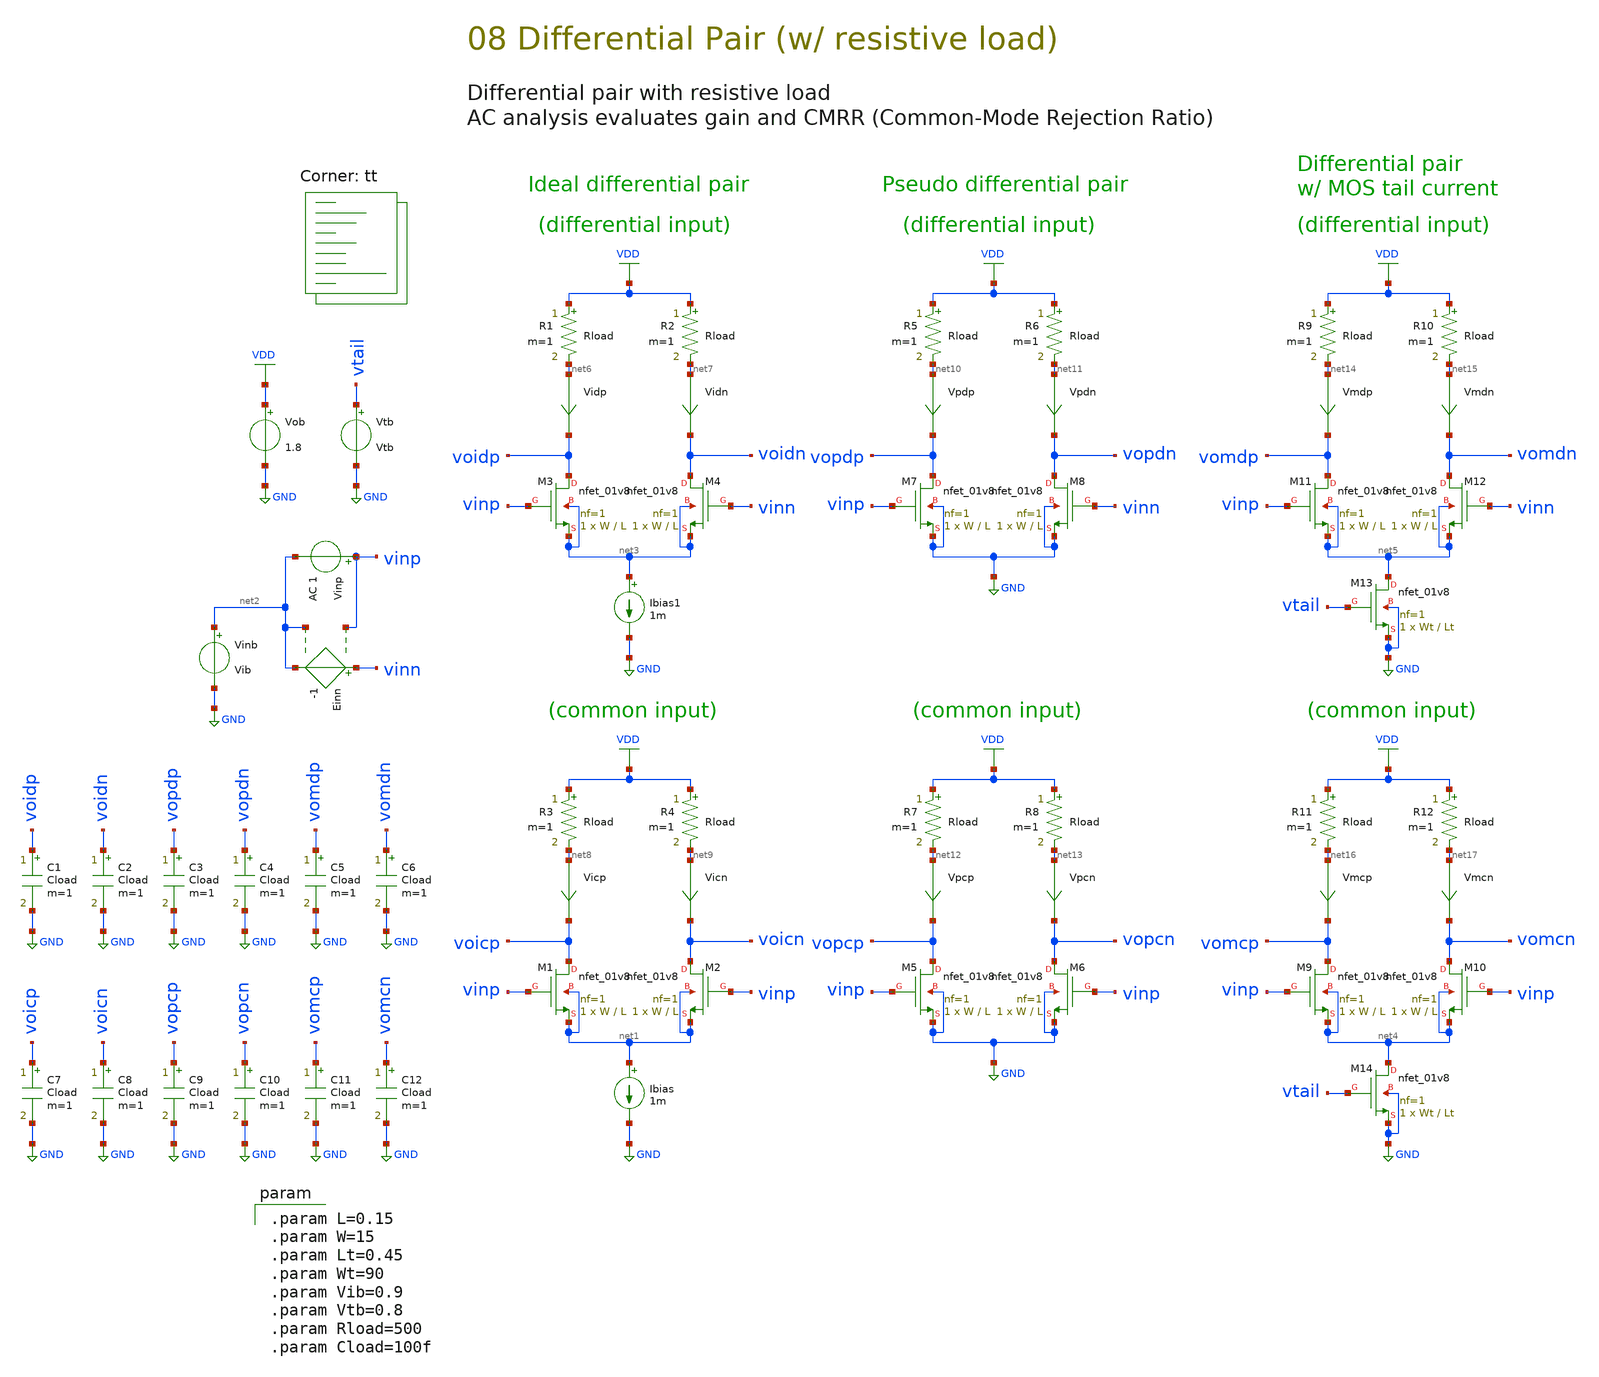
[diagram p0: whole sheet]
** sch_path: 08-b_diff-pair.sch
**.subckt 08-b_diff-pair
Vob VDD GND 1.8
XM1 voicp vinp net1 net1 sky130_fd_pr__nfet_01v8 L=L W=W nf=1 ad='int((1 + 1)/2) * W / 1 * 0.29' as='int((1 + 2)/2) * W / 1 * 0.29'
+ pd='2*int((1 + 1)/2) * (W / 1 + 0.29)' ps='2*int((1 + 2)/2) * (W / 1 + 0.29)' nrd='0.29 / W ' nrs='0.29 / W '
+ sa=0 sb=0 sd=0 mult=1 m=1
Vicn net9 voicn 0
.save i(vicn)
XM2 voicn vinp net1 net1 sky130_fd_pr__nfet_01v8 L=L W=W nf=1 ad='int((1 + 1)/2) * W / 1 * 0.29' as='int((1 + 2)/2) * W / 1 * 0.29'
+ pd='2*int((1 + 1)/2) * (W / 1 + 0.29)' ps='2*int((1 + 2)/2) * (W / 1 + 0.29)' nrd='0.29 / W ' nrs='0.29 / W '
+ sa=0 sb=0 sd=0 mult=1 m=1
Vinb net2 GND Vib
Vinp vinp net2 AC 1
Vicp net8 voicp 0
.save i(vicp)
Ibias net1 GND 1m
Einn vinn net2 vinp net2 -1
XM3 voidp vinp net3 net3 sky130_fd_pr__nfet_01v8 L=L W=W nf=1 ad='int((1 + 1)/2) * W / 1 * 0.29' as='int((1 + 2)/2) * W / 1 * 0.29'
+ pd='2*int((1 + 1)/2) * (W / 1 + 0.29)' ps='2*int((1 + 2)/2) * (W / 1 + 0.29)' nrd='0.29 / W ' nrs='0.29 / W '
+ sa=0 sb=0 sd=0 mult=1 m=1
Vidn net7 voidn 0
.save i(vidn)
XM4 voidn vinn net3 net3 sky130_fd_pr__nfet_01v8 L=L W=W nf=1 ad='int((1 + 1)/2) * W / 1 * 0.29' as='int((1 + 2)/2) * W / 1 * 0.29'
+ pd='2*int((1 + 1)/2) * (W / 1 + 0.29)' ps='2*int((1 + 2)/2) * (W / 1 + 0.29)' nrd='0.29 / W ' nrs='0.29 / W '
+ sa=0 sb=0 sd=0 mult=1 m=1
Vidp net6 voidp 0
.save i(vidp)
Ibias1 net3 GND 1m
XM5 vopcp vinp GND GND sky130_fd_pr__nfet_01v8 L=L W=W nf=1 ad='int((1 + 1)/2) * W / 1 * 0.29' as='int((1 + 2)/2) * W / 1 * 0.29'
+ pd='2*int((1 + 1)/2) * (W / 1 + 0.29)' ps='2*int((1 + 2)/2) * (W / 1 + 0.29)' nrd='0.29 / W ' nrs='0.29 / W '
+ sa=0 sb=0 sd=0 mult=1 m=1
Vpcn net13 vopcn 0
.save i(vpcn)
XM6 vopcn vinp GND GND sky130_fd_pr__nfet_01v8 L=L W=W nf=1 ad='int((1 + 1)/2) * W / 1 * 0.29' as='int((1 + 2)/2) * W / 1 * 0.29'
+ pd='2*int((1 + 1)/2) * (W / 1 + 0.29)' ps='2*int((1 + 2)/2) * (W / 1 + 0.29)' nrd='0.29 / W ' nrs='0.29 / W '
+ sa=0 sb=0 sd=0 mult=1 m=1
Vpcp net12 vopcp 0
.save i(vpcp)
XM7 vopdp vinp GND GND sky130_fd_pr__nfet_01v8 L=L W=W nf=1 ad='int((1 + 1)/2) * W / 1 * 0.29' as='int((1 + 2)/2) * W / 1 * 0.29'
+ pd='2*int((1 + 1)/2) * (W / 1 + 0.29)' ps='2*int((1 + 2)/2) * (W / 1 + 0.29)' nrd='0.29 / W ' nrs='0.29 / W '
+ sa=0 sb=0 sd=0 mult=1 m=1
Vpdn net11 vopdn 0
.save i(vpdn)
XM8 vopdn vinn GND GND sky130_fd_pr__nfet_01v8 L=L W=W nf=1 ad='int((1 + 1)/2) * W / 1 * 0.29' as='int((1 + 2)/2) * W / 1 * 0.29'
+ pd='2*int((1 + 1)/2) * (W / 1 + 0.29)' ps='2*int((1 + 2)/2) * (W / 1 + 0.29)' nrd='0.29 / W ' nrs='0.29 / W '
+ sa=0 sb=0 sd=0 mult=1 m=1
Vpdp net10 vopdp 0
.save i(vpdp)
XM9 vomcp vinp net4 net4 sky130_fd_pr__nfet_01v8 L=L W=W nf=1 ad='int((1 + 1)/2) * W / 1 * 0.29' as='int((1 + 2)/2) * W / 1 * 0.29'
+ pd='2*int((1 + 1)/2) * (W / 1 + 0.29)' ps='2*int((1 + 2)/2) * (W / 1 + 0.29)' nrd='0.29 / W ' nrs='0.29 / W '
+ sa=0 sb=0 sd=0 mult=1 m=1
Vmcn net17 vomcn 0
.save i(vmcn)
XM10 vomcn vinp net4 net4 sky130_fd_pr__nfet_01v8 L=L W=W nf=1 ad='int((1 + 1)/2) * W / 1 * 0.29' as='int((1 + 2)/2) * W / 1 * 0.29'
+ pd='2*int((1 + 1)/2) * (W / 1 + 0.29)' ps='2*int((1 + 2)/2) * (W / 1 + 0.29)' nrd='0.29 / W ' nrs='0.29 / W '
+ sa=0 sb=0 sd=0 mult=1 m=1
Vmcp net16 vomcp 0
.save i(vmcp)
XM11 vomdp vinp net5 net5 sky130_fd_pr__nfet_01v8 L=L W=W nf=1 ad='int((1 + 1)/2) * W / 1 * 0.29' as='int((1 + 2)/2) * W / 1 * 0.29'
+ pd='2*int((1 + 1)/2) * (W / 1 + 0.29)' ps='2*int((1 + 2)/2) * (W / 1 + 0.29)' nrd='0.29 / W ' nrs='0.29 / W '
+ sa=0 sb=0 sd=0 mult=1 m=1
Vmdn net15 vomdn 0
.save i(vmdn)
XM12 vomdn vinn net5 net5 sky130_fd_pr__nfet_01v8 L=L W=W nf=1 ad='int((1 + 1)/2) * W / 1 * 0.29' as='int((1 + 2)/2) * W / 1 * 0.29'
+ pd='2*int((1 + 1)/2) * (W / 1 + 0.29)' ps='2*int((1 + 2)/2) * (W / 1 + 0.29)' nrd='0.29 / W ' nrs='0.29 / W '
+ sa=0 sb=0 sd=0 mult=1 m=1
Vmdp net14 vomdp 0
.save i(vmdp)
XM13 net5 vtail GND GND sky130_fd_pr__nfet_01v8 L=Lt W=Wt nf=1 ad='int((1 + 1)/2) * Wt / 1 * 0.29' as='int((1 + 2)/2) * Wt / 1 * 0.29'
+ pd='2*int((1 + 1)/2) * (Wt / 1 + 0.29)' ps='2*int((1 + 2)/2) * (Wt / 1 + 0.29)' nrd='0.29 / Wt ' nrs='0.29 / Wt '
+ sa=0 sb=0 sd=0 mult=1 m=1
Vtb vtail GND Vtb
XM14 net4 vtail GND GND sky130_fd_pr__nfet_01v8 L=Lt W=Wt nf=1 ad='int((1 + 1)/2) * Wt / 1 * 0.29' as='int((1 + 2)/2) * Wt / 1 * 0.29'
+ pd='2*int((1 + 1)/2) * (Wt / 1 + 0.29)' ps='2*int((1 + 2)/2) * (Wt / 1 + 0.29)' nrd='0.29 / Wt ' nrs='0.29 / Wt '
+ sa=0 sb=0 sd=0 mult=1 m=1
R1 VDD net6 Rload m=1
R2 VDD net7 Rload m=1
R3 VDD net8 Rload m=1
R4 VDD net9 Rload m=1
R5 VDD net10 Rload m=1
R6 VDD net11 Rload m=1
R7 VDD net12 Rload m=1
R8 VDD net13 Rload m=1
R9 VDD net14 Rload m=1
R10 VDD net15 Rload m=1
R11 VDD net16 Rload m=1
R12 VDD net17 Rload m=1
C1 voidp GND Cload m=1
C2 voidn GND Cload m=1
C3 vopdp GND Cload m=1
C4 vopdn GND Cload m=1
C5 vomdp GND Cload m=1
C6 vomdn GND Cload m=1
C7 voicp GND Cload m=1
C8 voicn GND Cload m=1
C9 vopcp GND Cload m=1
C10 vopcn GND Cload m=1
C11 vomcp GND Cload m=1
C12 vomcn GND Cload m=1
**** begin user architecture code
.lib $::SKYWATER_MODELS/sky130.lib.spice tt

.param L=0.15
.param W=15
.param Lt=0.45
.param Wt=90
.param Vib=0.9
.param Vtb=0.8
.param Rload=500
.param Cload=100f


.option savecurrent
.control
save all

* DC analysis (IO curve)
dc Vinp -0.9 0.9 0.01
plot voidp voidn
plot voicp voicn
plot vopdp vopdn
plot vopcp vopcn
plot vomdp vomdn
plot vomcp vomcn

* AC analysis (gain and CMRR)
ac dec 20 1e6 1e10
plot Vdb(voidp) Vdb(voicp)
plot Vdb(vopdp) Vdb(vopcp)
plot Vdb(vomdp) Vdb(vomcp)
plot Vdb(voidp)-Vdb(voicp) Vdb(vopdp)-Vdb(vopcp) Vdb(vomdp)-Vdb(vomcp)
.endc

**** end user architecture code
**.ends
.GLOBAL GND
.GLOBAL VDD
.end
